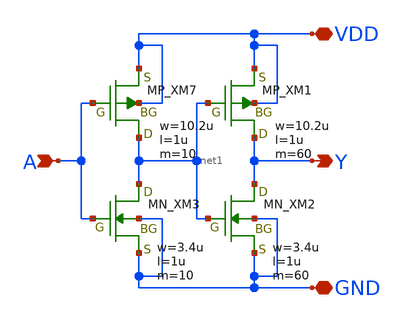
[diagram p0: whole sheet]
** sch_path: openIP62_rev1.0/IP62/Technology/tech/symbols/Xschem/IP62_5_stdcell/CLKBUF_X12.sch
**.subckt CLKBUF_X12 A Y VDD GND
*.ipin A
*.opin Y
*.iopin VDD
*.iopin GND
XM7 net1 A VDD VDD PMOS w=10.2u l=1u as=0 ad=0 ps=0 pd=0 nrd=0 nrs=0 m=10
XM1 Y net1 VDD VDD PMOS w=10.2u l=1u as=0 ad=0 ps=0 pd=0 nrd=0 nrs=0 m=60
XM3 net1 A GND GND NMOS w=3.4u l=1u as=0 ad=0 ps=0 pd=0 nrd=0 nrs=0 m=10
XM2 Y net1 GND GND NMOS w=3.4u l=1u as=0 ad=0 ps=0 pd=0 nrd=0 nrs=0 m=60
**.ends
.end
